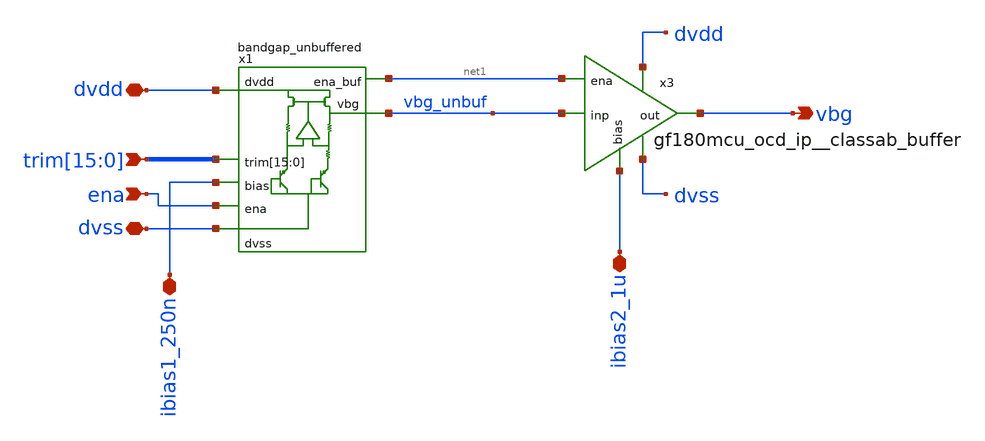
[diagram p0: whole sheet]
** sch_path: projects/programmable_transceiver_platform/analog/core_support/bandgap/xschem/gf180mcu_ocd_ip__bandgap.sch
**.subckt gf180mcu_ocd_ip__bandgap
*+ trim[15],trim[14],trim[13],trim[12],trim[11],trim[10],trim[9],trim[8],trim[7],trim[6],trim[5],trim[4],trim[3],trim[2],trim[1],trim[0] ena vbg ibias2_1u ibias1_250n dvdd dvss
*.ipin
*+ trim[15],trim[14],trim[13],trim[12],trim[11],trim[10],trim[9],trim[8],trim[7],trim[6],trim[5],trim[4],trim[3],trim[2],trim[1],trim[0]
*.ipin ena
*.opin vbg
*.iopin ibias2_1u
*.iopin ibias1_250n
*.iopin dvdd
*.iopin dvss
x1 vbg_unbuf ibias1_250n trim[15] trim[14] trim[13] trim[12] trim[11] trim[10] trim[9] trim[8]
+ trim[7] trim[6] trim[5] trim[4] trim[3] trim[2] trim[1] trim[0] dvss dvdd ena net1 bandgap_unbuffered
x3 dvdd vbg vbg_unbuf dvss ibias2_1u net1 gf180mcu_ocd_ip__classab_buffer
**.ends
.end
